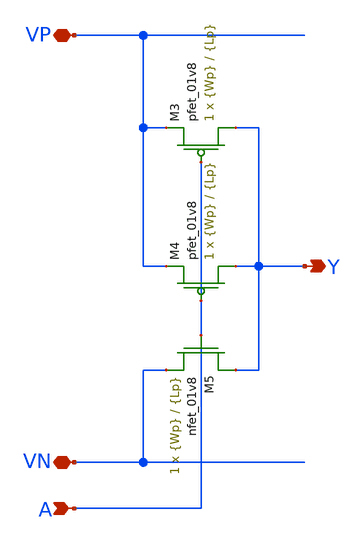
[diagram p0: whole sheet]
** sch_path: schematic/inverter.sch
**.subckt inverter Y A VP VN
*.opin Y
*.ipin A
*.iopin VP
*.iopin VN
XM3 Y A VP VDD sky130_fd_pr__pfet_01v8 L={Lp} W={Wp} nf=1 ad='int((nf+1)/2) * W/nf * 0.29' as='int((nf+2)/2) * W/nf * 0.29'
+ pd='2*int((nf+1)/2) * (W/nf + 0.29)' ps='2*int((nf+2)/2) * (W/nf + 0.29)' nrd='0.29 / W' nrs='0.29 / W'
+ sa=0 sb=0 sd=0 mult=1 m=1
XM4 Y A VP VDD sky130_fd_pr__pfet_01v8 L={Lp} W={Wp} nf=1 ad='int((nf+1)/2) * W/nf * 0.29' as='int((nf+2)/2) * W/nf * 0.29'
+ pd='2*int((nf+1)/2) * (W/nf + 0.29)' ps='2*int((nf+2)/2) * (W/nf + 0.29)' nrd='0.29 / W' nrs='0.29 / W'
+ sa=0 sb=0 sd=0 mult=1 m=1
XM5 Y A VN GND sky130_fd_pr__nfet_01v8 L={Lp} W={Wp} nf=1 ad='int((nf+1)/2) * W/nf * 0.29' as='int((nf+2)/2) * W/nf * 0.29'
+ pd='2*int((nf+1)/2) * (W/nf + 0.29)' ps='2*int((nf+2)/2) * (W/nf + 0.29)' nrd='0.29 / W' nrs='0.29 / W'
+ sa=0 sb=0 sd=0 mult=1 m=1
**.ends
.end
